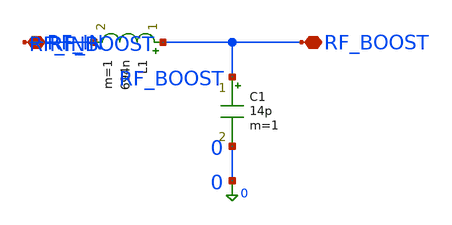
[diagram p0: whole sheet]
** sch_path: modules/PandaChip/designs/iris-harvester/exp/matching.sch
**.subckt matching RF_IN RF_BOOST
*.iopin RF_IN
*.iopin RF_BOOST
L1 RF_BOOST RF_IN 694n m=1
C1 RF_BOOST 0 14p m=1
**.ends
.end
